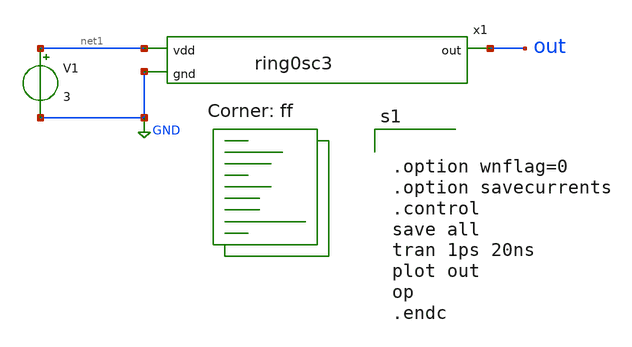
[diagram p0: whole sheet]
** sch_path: ring_osilator/ring0sc3_tb.sch
**.subckt ring0sc3_tb
x1 net1 out GND ring0sc3
V1 net1 GND 3
**** begin user architecture code
.lib $::SKYWATER_MODELS/sky130.lib.spice ff


.option wnflag=0
.option savecurrents
.control
save all
tran 1ps 20ns
plot out
op
.endc


**** end user architecture code
**.ends
.GLOBAL GND
.end
